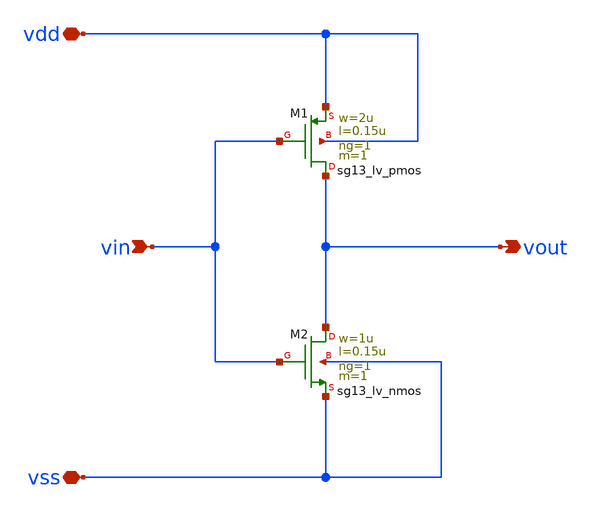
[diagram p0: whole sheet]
** sch_path: Designs/Analog_Inverter/Schematics/Analog_Inverter.sch
* (c) 2024 Hrishikesh, @HSB
**.subckt Analog_Inverter vin vdd vss vout
*.ipin vin
*.iopin vdd
*.iopin vss
*.opin vout
XM1 vout vin vdd vdd sg13_lv_pmos w=2u l=0.15u ng=1 m=1 mm_ok=1
XM2 vout vin vss vss sg13_lv_nmos w=1u l=0.15u ng=1 m=1 mm_ok=1
**.ends
.end
